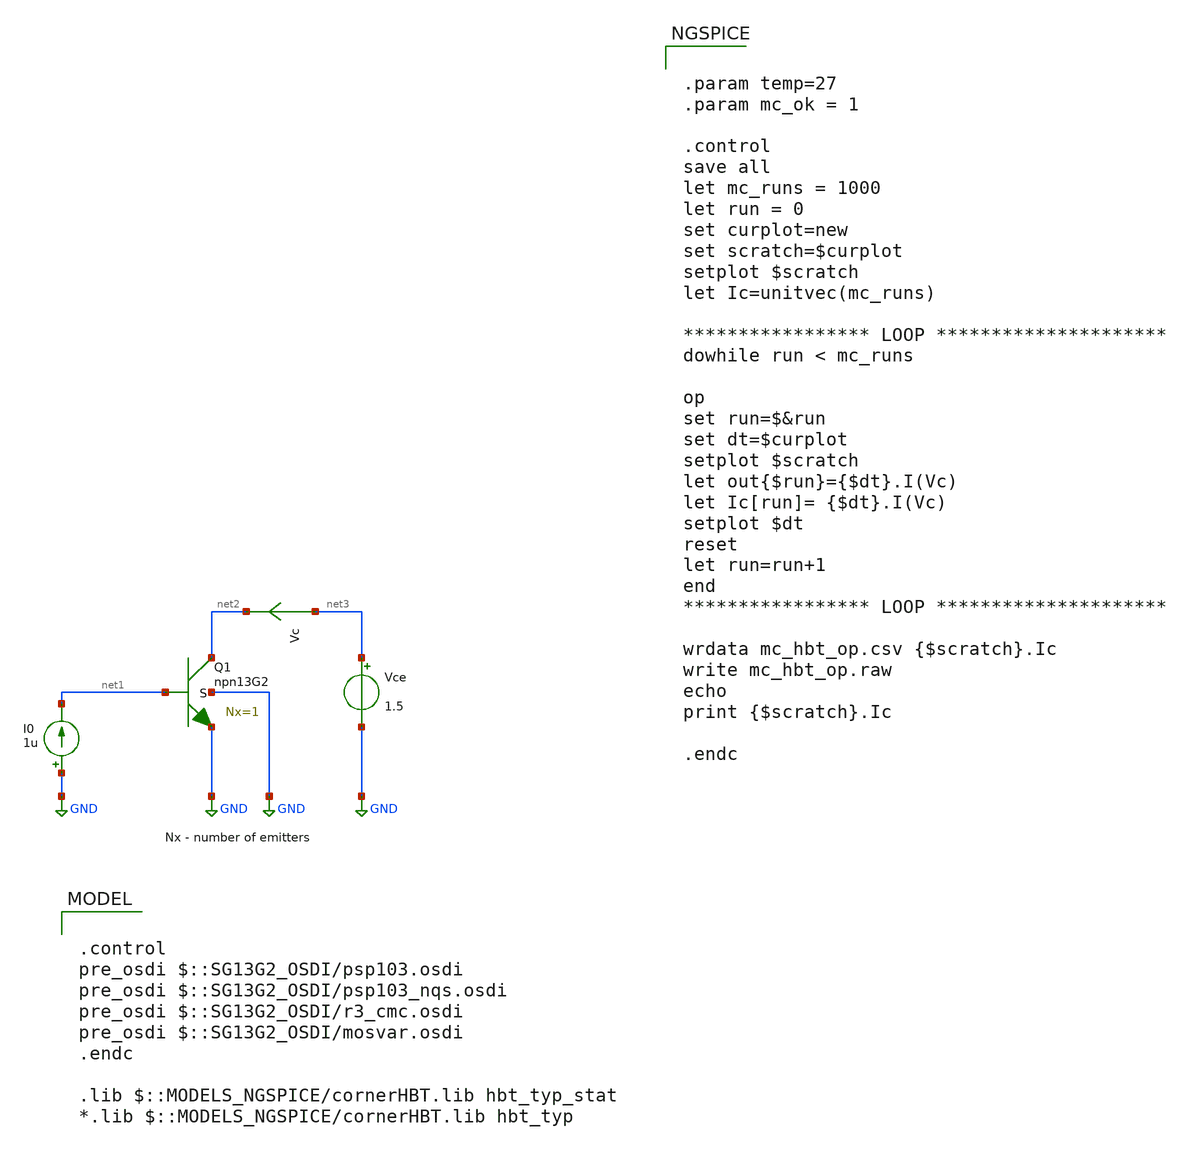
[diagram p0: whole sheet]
** sch_path: ihp-sg13g2/xschem_libs/sg13g2_tests/mc_hbt_13g2/schematic/mc_hbt_13g2.sch
* Copyright 2023 IHP PDK Authors
**.subckt mc_hbt_13g2
Vce net3 GND 1.5
I0 GND net1 1u
Vc net3 net2 0
.save i(vc)
XQ1 net2 net1 GND GND npn13G2 Nx=1 mm_ok=1
**** begin user architecture code

.control
pre_osdi $::SG13G2_OSDI/psp103.osdi
pre_osdi $::SG13G2_OSDI/psp103_nqs.osdi
pre_osdi $::SG13G2_OSDI/r3_cmc.osdi
pre_osdi $::SG13G2_OSDI/mosvar.osdi
.endc

.lib $::MODELS_NGSPICE/cornerHBT.lib hbt_typ_stat
*.lib $::MODELS_NGSPICE/cornerHBT.lib hbt_typ



.param temp=27
.param mc_ok = 1

.control
save all
let mc_runs = 1000
let run = 0
set curplot=new
set scratch=$curplot
setplot $scratch
let Ic=unitvec(mc_runs)

***************** LOOP *********************
dowhile run < mc_runs

op
set run=$&run
set dt=$curplot
setplot $scratch
let out{$run}={$dt}.I(Vc)
let Ic[run]= {$dt}.I(Vc)
setplot $dt
reset
let run=run+1
end
***************** LOOP *********************

wrdata mc_hbt_op.csv {$scratch}.Ic
write mc_hbt_op.raw
echo
print {$scratch}.Ic

.endc


**** end user architecture code
**.ends
.GLOBAL GND
.end
